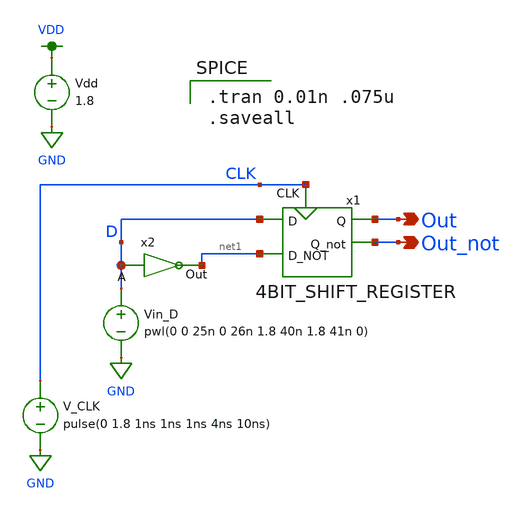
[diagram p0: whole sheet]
** sch_path: miniproject2/MP2_LAB.sch
**.subckt MP2_LAB Out Out_not
*.opin Out
*.opin Out_not
x1 CLK D Out Out_not net1 4BIT_SHIFT_REGISTER
Vin_D D GND pwl(0 0 25n 0 26n 1.8 40n 1.8 41n 0)
V_CLK CLK GND pulse(0 1.8 1ns 1ns 1ns 4ns 10ns)
Vdd VDD GND 1.8
x2 net1 D MP1_inverter
**** begin user architecture code

.tran 0.01n .075u
.saveall


.option wnflag=1
.lib ~/skywater/skywater-pdk/libraries/sky130_fd_pr_ngspice/latest/models/sky130.lib.spice tt

**** end user architecture code
**.ends

* expanding   symbol:  /home/lxbtlr/MAD/miniproject2/4BIT_SHIFT_REGISTER.sym # of pins=5
** sym_path: miniproject2/4BIT_SHIFT_REGISTER.sym
** sch_path: miniproject2/4BIT_SHIFT_REGISTER.sch
.subckt 4BIT_SHIFT_REGISTER CLK D Q Q_not D_NOT
*.opin Q
*.opin Q_not
*.ipin D
*.ipin D_NOT
*.ipin CLK
x1 D Q1 D_NOT net3 CLK CSRL_Latch
x2 Q1 Q2 net3 net2 CLK CSRL_Latch
x3 Q2 Q3 net2 net1 CLK CSRL_Latch
x4 Q3 Q net1 Q_not CLK CSRL_Latch
.ends


* expanding   symbol:  /home/lxbtlr/MAD/miniproject1/MP1_inverter.sym # of pins=2
** sym_path: miniproject2/MP1_inverter.sym
** sch_path: miniproject2/MP1_inverter.sch
.subckt MP1_inverter Out A
*.ipin A
*.opin Out
XM1 Out A VDD VDD sky130_fd_pr__pfet_01v8 L=0.15 W=1 nf=1 ad='int((nf+1)/2) * W/nf * 0.29' as='int((nf+2)/2) * W/nf * 0.29'
+ pd='2*int((nf+1)/2) * (W/nf + 0.29)' ps='2*int((nf+2)/2) * (W/nf + 0.29)' nrd='0.29 / W' nrs='0.29 / W'
+ sa=0 sb=0 sd=0 mult=1 m=1
XM2 Out A GND GND sky130_fd_pr__nfet_01v8 L=0.15 W=1 nf=1 ad='int((nf+1)/2) * W/nf * 0.29' as='int((nf+2)/2) * W/nf * 0.29'
+ pd='2*int((nf+1)/2) * (W/nf + 0.29)' ps='2*int((nf+2)/2) * (W/nf + 0.29)' nrd='0.29 / W' nrs='0.29 / W'
+ sa=0 sb=0 sd=0 mult=1 m=1
.ends


* expanding   symbol:  /home/lxbtlr/MAD/miniproject2/CSRL_Latch.sym # of pins=5
** sym_path: miniproject2/CSRL_Latch.sym
** sch_path: miniproject2/CSRL_Latch.sch
.subckt CSRL_Latch D Q D_NOT Q_NOT CLK
*.ipin D
*.ipin D_NOT
*.opin Q
*.opin Q_NOT
*.ipin CLK
XQ8 net2 net3 VDD VDD sky130_fd_pr__pfet_01v8 L=0.15 W=1 nf=1 ad='int((nf+1)/2) * W/nf * 0.29' as='int((nf+2)/2) * W/nf * 0.29'
+ pd='2*int((nf+1)/2) * (W/nf + 0.29)' ps='2*int((nf+2)/2) * (W/nf + 0.29)' nrd='0.29 / W' nrs='0.29 / W'
+ sa=0 sb=0 sd=0 mult=1 m=1
XQ9 VDD net2 net3 VDD sky130_fd_pr__pfet_01v8 L=0.15 W=1 nf=1 ad='int((nf+1)/2) * W/nf * 0.29' as='int((nf+2)/2) * W/nf * 0.29'
+ pd='2*int((nf+1)/2) * (W/nf + 0.29)' ps='2*int((nf+2)/2) * (W/nf + 0.29)' nrd='0.29 / W' nrs='0.29 / W'
+ sa=0 sb=0 sd=0 mult=1 m=1
XQ1 net3 CLK D VDD sky130_fd_pr__pfet_01v8 L=0.15 W=1 nf=1 ad='int((nf+1)/2) * W/nf * 0.29' as='int((nf+2)/2) * W/nf * 0.29'
+ pd='2*int((nf+1)/2) * (W/nf + 0.29)' ps='2*int((nf+2)/2) * (W/nf + 0.29)' nrd='0.29 / W' nrs='0.29 / W'
+ sa=0 sb=0 sd=0 mult=1 m=1
XQ2 net2 CLK D_NOT VDD sky130_fd_pr__pfet_01v8 L=0.15 W=1 nf=1 ad='int((nf+1)/2) * W/nf * 0.29' as='int((nf+2)/2) * W/nf * 0.29'
+ pd='2*int((nf+1)/2) * (W/nf + 0.29)' ps='2*int((nf+2)/2) * (W/nf + 0.29)' nrd='0.29 / W' nrs='0.29 / W'
+ sa=0 sb=0 sd=0 mult=1 m=1
XQ5 net1 CLK GND GND sky130_fd_pr__nfet_01v8 L=0.15 W=4 nf=1 ad='int((nf+1)/2) * W/nf * 0.29' as='int((nf+2)/2) * W/nf * 0.29'
+ pd='2*int((nf+1)/2) * (W/nf + 0.29)' ps='2*int((nf+2)/2) * (W/nf + 0.29)' nrd='0.29 / W' nrs='0.29 / W'
+ sa=0 sb=0 sd=0 mult=1 m=1
XQ4 Q_NOT CLK net2 GND sky130_fd_pr__nfet_01v8 L=0.15 W=1 nf=1 ad='int((nf+1)/2) * W/nf * 0.29' as='int((nf+2)/2) * W/nf * 0.29'
+ pd='2*int((nf+1)/2) * (W/nf + 0.29)' ps='2*int((nf+2)/2) * (W/nf + 0.29)' nrd='0.29 / W' nrs='0.29 / W'
+ sa=0 sb=0 sd=0 mult=1 m=1
XQ3 Q CLK net3 GND sky130_fd_pr__nfet_01v8 L=0.15 W=1 nf=1 ad='int((nf+1)/2) * W/nf * 0.29' as='int((nf+2)/2) * W/nf * 0.29'
+ pd='2*int((nf+1)/2) * (W/nf + 0.29)' ps='2*int((nf+2)/2) * (W/nf + 0.29)' nrd='0.29 / W' nrs='0.29 / W'
+ sa=0 sb=0 sd=0 mult=1 m=1
XQ6 net2 net3 net1 GND sky130_fd_pr__nfet_01v8 L=0.15 W=1 nf=1 ad='int((nf+1)/2) * W/nf * 0.29' as='int((nf+2)/2) * W/nf * 0.29'
+ pd='2*int((nf+1)/2) * (W/nf + 0.29)' ps='2*int((nf+2)/2) * (W/nf + 0.29)' nrd='0.29 / W' nrs='0.29 / W'
+ sa=0 sb=0 sd=0 mult=1 m=1
XQ7 net1 net2 net3 GND sky130_fd_pr__nfet_01v8 L=0.15 W=1 nf=1 ad='int((nf+1)/2) * W/nf * 0.29' as='int((nf+2)/2) * W/nf * 0.29'
+ pd='2*int((nf+1)/2) * (W/nf + 0.29)' ps='2*int((nf+2)/2) * (W/nf + 0.29)' nrd='0.29 / W' nrs='0.29 / W'
+ sa=0 sb=0 sd=0 mult=1 m=1
XQ13 Q_NOT Q GND GND sky130_fd_pr__nfet_01v8 L=0.15 W=1 nf=1 ad='int((nf+1)/2) * W/nf * 0.29' as='int((nf+2)/2) * W/nf * 0.29'
+ pd='2*int((nf+1)/2) * (W/nf + 0.29)' ps='2*int((nf+2)/2) * (W/nf + 0.29)' nrd='0.29 / W' nrs='0.29 / W'
+ sa=0 sb=0 sd=0 mult=1 m=1
XQ14 GND Q_NOT Q GND sky130_fd_pr__nfet_01v8 L=0.15 W=1 nf=1 ad='int((nf+1)/2) * W/nf * 0.29' as='int((nf+2)/2) * W/nf * 0.29'
+ pd='2*int((nf+1)/2) * (W/nf + 0.29)' ps='2*int((nf+2)/2) * (W/nf + 0.29)' nrd='0.29 / W' nrs='0.29 / W'
+ sa=0 sb=0 sd=0 mult=1 m=1
XQ11 Q_NOT Q net4 VDD sky130_fd_pr__pfet_01v8 L=0.15 W=1 nf=1 ad='int((nf+1)/2) * W/nf * 0.29' as='int((nf+2)/2) * W/nf * 0.29'
+ pd='2*int((nf+1)/2) * (W/nf + 0.29)' ps='2*int((nf+2)/2) * (W/nf + 0.29)' nrd='0.29 / W' nrs='0.29 / W'
+ sa=0 sb=0 sd=0 mult=1 m=1
XQ12 net4 Q_NOT Q VDD sky130_fd_pr__pfet_01v8 L=0.15 W=1 nf=1 ad='int((nf+1)/2) * W/nf * 0.29' as='int((nf+2)/2) * W/nf * 0.29'
+ pd='2*int((nf+1)/2) * (W/nf + 0.29)' ps='2*int((nf+2)/2) * (W/nf + 0.29)' nrd='0.29 / W' nrs='0.29 / W'
+ sa=0 sb=0 sd=0 mult=1 m=1
XQ10 net4 CLK VDD VDD sky130_fd_pr__pfet_01v8 L=0.15 W=4 nf=1 ad='int((nf+1)/2) * W/nf * 0.29' as='int((nf+2)/2) * W/nf * 0.29'
+ pd='2*int((nf+1)/2) * (W/nf + 0.29)' ps='2*int((nf+2)/2) * (W/nf + 0.29)' nrd='0.29 / W' nrs='0.29 / W'
+ sa=0 sb=0 sd=0 mult=1 m=1
.ends

.GLOBAL GND
.GLOBAL VDD
.end
